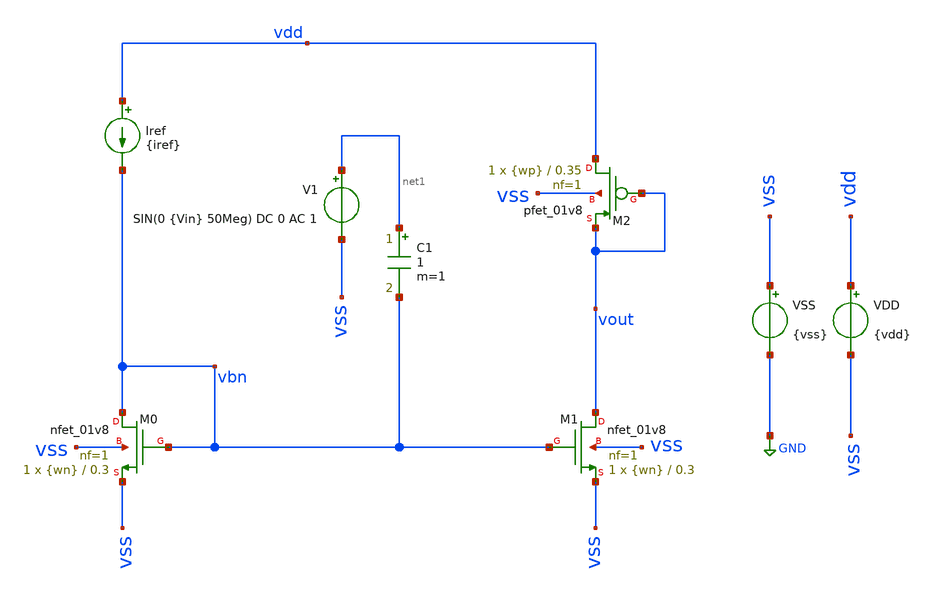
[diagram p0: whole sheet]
** sch_path: TP2/tp2_6.sch
**.subckt tp2_6
Iref vdd vbn {iref}
VSS vss GND {vss}
VDD vdd vss {vdd}
V1 net1 vss SIN(0 {Vin} 50Meg) DC 0 AC 1
XM1 vout vbn vss vss sky130_fd_pr__nfet_01v8 L=0.3 W={wn} nf=1 ad='int((nf+1)/2) * W/nf * 0.29' as='int((nf+2)/2) * W/nf * 0.29'
+ pd='2*int((nf+1)/2) * (W/nf + 0.29)' ps='2*int((nf+2)/2) * (W/nf + 0.29)' nrd='0.29 / W' nrs='0.29 / W'
+ sa=0 sb=0 sd=0 mult=1 m=1
XM0 vbn vbn vss vss sky130_fd_pr__nfet_01v8 L=0.3 W={wn} nf=1 ad='int((nf+1)/2) * W/nf * 0.29' as='int((nf+2)/2) * W/nf * 0.29'
+ pd='2*int((nf+1)/2) * (W/nf + 0.29)' ps='2*int((nf+2)/2) * (W/nf + 0.29)' nrd='0.29 / W' nrs='0.29 / W'
+ sa=0 sb=0 sd=0 mult=1 m=1
C1 net1 vbn 1 m=1
XM2 vdd vout vout vss sky130_fd_pr__pfet_01v8 L=0.35 W={wp} nf=1 ad='int((nf+1)/2) * W/nf * 0.29' as='int((nf+2)/2) * W/nf * 0.29'
+ pd='2*int((nf+1)/2) * (W/nf + 0.29)' ps='2*int((nf+2)/2) * (W/nf + 0.29)' nrd='0.29 / W' nrs='0.29 / W'
+ sa=0 sb=0 sd=0 mult=1 m=1
**** begin user architecture code



* Parameters
.param vdd = 1.8
.param vss = 0.0
.param iref = 200u
.param wn = 6.5
.param wp = 35
.param Vin = 40m

.options TEMP = 65.0

* Models
.lib ~/skywater/skywater-pdk/libraries/sky130_fd_pr_ngspice/latest/models/corners/sky130.lib TT

* Data to save
.save all  @M.XM0.msky130_fd_pr__nfet_01v8[id]  @M.XM0.msky130_fd_pr__nfet_01v8[vds]  @M.XM0.msky130_fd_pr__nfet_01v8[vgs]  @M.XM0.msky130_fd_pr__nfet_01v8[vdsat]  @M.XM0.msky130_fd_pr__nfet_01v8[vth]  @M.XM0.msky130_fd_pr__nfet_01v8[gm]  @M.XM1.msky130_fd_pr__nfet_01v8[id]  @M.XM1.msky130_fd_pr__nfet_01v8[vds]  @M.XM1.msky130_fd_pr__nfet_01v8[vgs]  @M.XM1.msky130_fd_pr__nfet_01v8[vdsat]  @M.XM1.msky130_fd_pr__nfet_01v8[vth]  @M.XM1.msky130_fd_pr__nfet_01v8[gm]  @M.XM1.msky130_fd_pr__nfet_01v8[gds]  @M.XM2.msky130_fd_pr__pfet_01v8[gm]


* Simulation
.control
  ac dec 100 10k 100G
  setplot ac1
  plot vdb(vout) {vp(vout)*180/PI}
  write tp2_5_ac.raw

  reset
  tran 0.01n 100n
  plot v(vbn) v(vout)
  write tp2_6_tran.raw

  reset
  op
  save all
  print all
  unset filetype
  write tp2_6.raw
.endc

.end


**** end user architecture code
**.ends
.GLOBAL GND
.end
